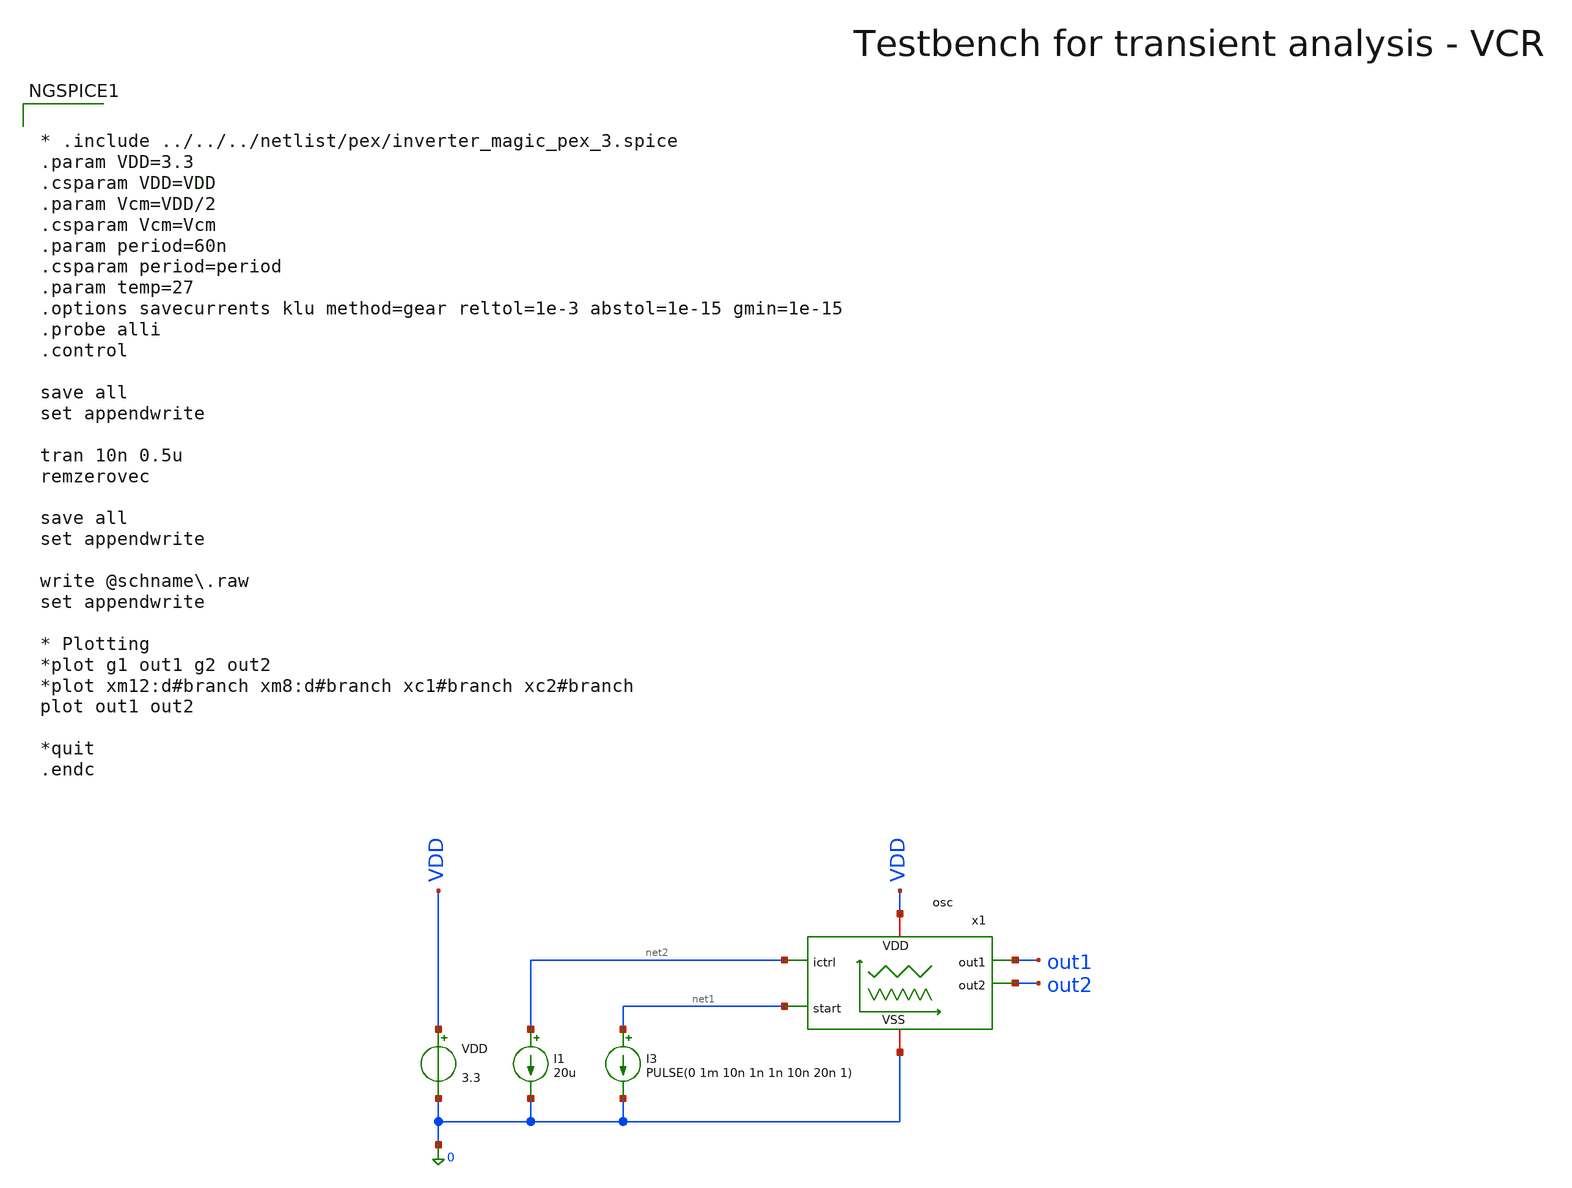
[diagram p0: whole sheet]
** sch_path: macros/heichips26_vcr/macros/switched_capacitor/testbenches/xschem/osc_tb_tran.sch
**.subckt osc_tb_tran
VDD VDD 0 3.3
I1 net2 0 20u
I3 net1 0 PULSE(0 1m 10n 1n 1n 10n 20n 1)
x1 VDD out1 net2 0 net1 out2 osc
**** begin user architecture code

.lib cornerMOSlv.lib mos_tt
.lib cornerMOShv.lib mos_tt
.lib cornerRES.lib res_typ
.lib cornerDIO.lib dio_tt
.lib cornerCAP.lib cap_typ

.include $::PDK_ROOT/$::PDK/libs.ref/sg13cmos5l_stdcell/spice/sg13cmos5l_stdcell.spice



* .include ../../../netlist/pex/inverter_magic_pex_3.spice
.param VDD=3.3
.csparam VDD=VDD
.param Vcm=VDD/2
.csparam Vcm=Vcm
.param period=60n
.csparam period=period
.param temp=27
.options savecurrents klu method=gear reltol=1e-3 abstol=1e-15 gmin=1e-15
.probe alli
.control

save all
set appendwrite

tran 10n 0.5u
remzerovec

save all
set appendwrite

write @schname\.raw
set appendwrite

* Plotting
*plot g1 out1 g2 out2
*plot xm12:d#branch xm8:d#branch xc1#branch xc2#branch
plot out1 out2

*quit
.endc


**** end user architecture code
**.ends

* expanding   symbol:  osc.sym # of pins=6
** sym_path: macros/heichips26_vcr/macros/switched_capacitor/schematic/xschem/osc.sym
** sch_path: macros/heichips26_vcr/macros/switched_capacitor/schematic/xschem/osc.sch
.subckt osc VDD out1 ictrl VSS start out2
*.iopin VSS
*.iopin VDD
*.iopin out2
*.iopin out1
*.iopin start
*.iopin ictrl
XM3 out1 ictrl VDD VDD sg13_hv_pmos w=10.0u l=2.0u ng=1 m=1 mm_ok=1
XM2 net1 ictrl VDD VDD sg13_hv_pmos w=1u l=2.0u ng=1 m=1 mm_ok=1
XM4 start ictrl VDD VDD sg13_hv_pmos w=1.0u l=2.0u ng=1 m=1 mm_ok=1
XM5 out2 ictrl VDD VDD sg13_hv_pmos w=10.0u l=2.0u ng=1 m=1 mm_ok=1
XM6 ictrl ictrl VDD VDD sg13_hv_pmos w=10.0u l=2.0u ng=1 m=1 mm_ok=1
XC1 net1 out1 cap_cmomi w=10e-6 l=10e-6 mmin=1 mmax=4 feed=double subblock=0 m=1 mm_ok=1
XC2 out2 start cap_cmomi w=10e-6 l=10e-6 mmin=1 mmax=4 feed=double subblock=0 m=1 mm_ok=1
XM8 out1 start VSS VSS sg13_hv_nmos w=3u l=0.45u ng=1 m=1 mm_ok=1
XM1 start start VSS VSS sg13_hv_nmos w=1u l=2u ng=1 m=1 mm_ok=1
XM12 out2 net1 VSS VSS sg13_hv_nmos w=3u l=0.45u ng=1 m=1 mm_ok=1
XM11 net1 net1 VSS VSS sg13_hv_nmos w=1u l=2u ng=1 m=1 mm_ok=1
**** begin user architecture code


.ic v(out1)=0 v(out2)=3.3


**** end user architecture code
.ends

.end
